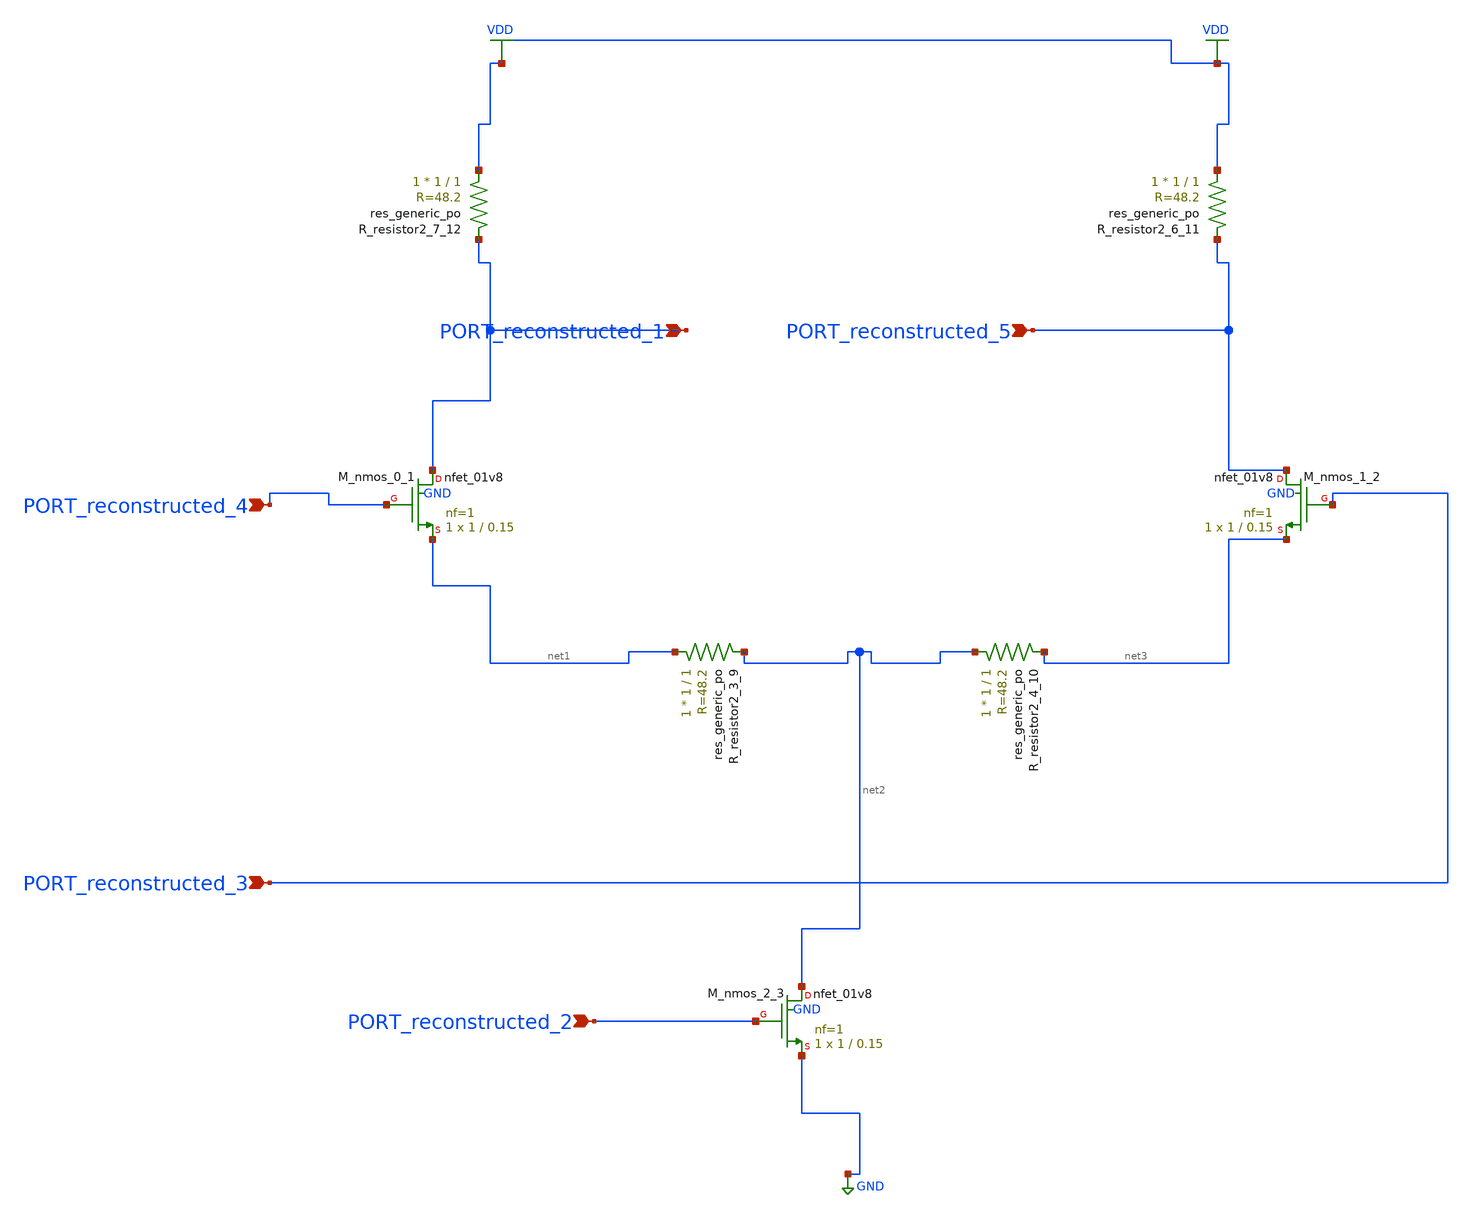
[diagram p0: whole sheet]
** sch_path: schematics/AMSNet/530.sch
**.subckt 530 PORT_reconstructed_1 PORT_reconstructed_2 PORT_reconstructed_3 PORT_reconstructed_4
*+ PORT_reconstructed_5
*.ipin PORT_reconstructed_1
*.ipin PORT_reconstructed_2
*.ipin PORT_reconstructed_3
*.ipin PORT_reconstructed_4
*.ipin PORT_reconstructed_5
XM_nmos_0_1 PORT_reconstructed_1 PORT_reconstructed_4 net1 GND sky130_fd_pr__nfet_01v8 L=0.15 W=1 nf=1
+ ad='int((1 + 1)/2) * 1 / 1 * 0.29' as='int((1 + 2)/2) * 1 / 1 * 0.29' pd='2*int((1 + 1)/2) * (1 / 1 + 0.29)'
+ ps='2*int((1 + 2)/2) * (1 / 1 + 0.29)' nrd='0.29 / 1 ' nrs='0.29 / 1 ' sa=0 sb=0 sd=0 mult=1 m=1
XM_nmos_1_2 PORT_reconstructed_5 PORT_reconstructed_3 net3 GND sky130_fd_pr__nfet_01v8 L=0.15 W=1 nf=1
+ ad='int((1 + 1)/2) * 1 / 1 * 0.29' as='int((1 + 2)/2) * 1 / 1 * 0.29' pd='2*int((1 + 1)/2) * (1 / 1 + 0.29)'
+ ps='2*int((1 + 2)/2) * (1 / 1 + 0.29)' nrd='0.29 / 1 ' nrs='0.29 / 1 ' sa=0 sb=0 sd=0 mult=1 m=1
XM_nmos_2_3 net2 PORT_reconstructed_2 GND GND sky130_fd_pr__nfet_01v8 L=0.15 W=1 nf=1 ad='int((1 + 1)/2) * 1 / 1 * 0.29'
+ as='int((1 + 2)/2) * 1 / 1 * 0.29' pd='2*int((1 + 1)/2) * (1 / 1 + 0.29)' ps='2*int((1 + 2)/2) * (1 / 1 + 0.29)'
+ nrd='0.29 / 1 ' nrs='0.29 / 1 ' sa=0 sb=0 sd=0 mult=1 m=1
XR_resistor2_3_9 net1 net2 sky130_fd_pr__res_generic_po W=1 L=1 m=1
XR_resistor2_4_10 net2 net3 sky130_fd_pr__res_generic_po W=1 L=1 m=1
XR_resistor2_6_11 VDD PORT_reconstructed_5 sky130_fd_pr__res_generic_po W=1 L=1 m=1
XR_resistor2_7_12 VDD PORT_reconstructed_1 sky130_fd_pr__res_generic_po W=1 L=1 m=1
**.ends
.GLOBAL GND
.GLOBAL VDD
.end
